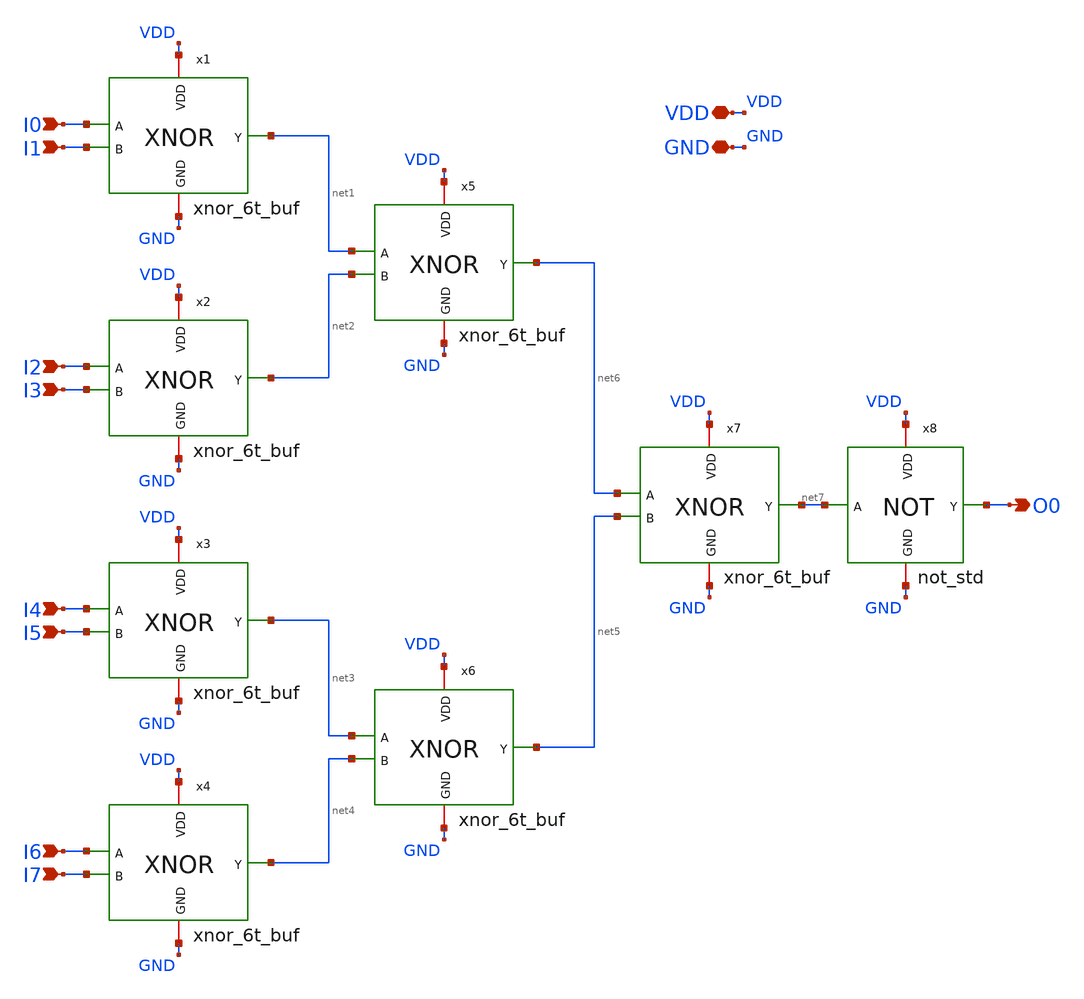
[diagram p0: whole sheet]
** sch_path: even_parity_generator/schematic/even_parity_gen_xnor_6t_buf.sch
**.subckt even_parity_gen_xnor_6t_buf VDD GND I0 I1 I2 I3 I4 I5 I6 I7 O0
*.iopin VDD
*.iopin GND
*.ipin I0
*.ipin I1
*.ipin I2
*.ipin I3
*.ipin I4
*.ipin I5
*.ipin I6
*.ipin I7
*.opin O0
x1 VDD I0 net1 I1 GND xnor_6t_buf
x2 VDD I2 net2 I3 GND xnor_6t_buf
x3 VDD I4 net3 I5 GND xnor_6t_buf
x4 VDD I6 net4 I7 GND xnor_6t_buf
x5 VDD net1 net6 net2 GND xnor_6t_buf
x6 VDD net3 net5 net4 GND xnor_6t_buf
x7 VDD net6 net7 net5 GND xnor_6t_buf
x8 VDD net7 O0 GND not_std
**.ends
.end
